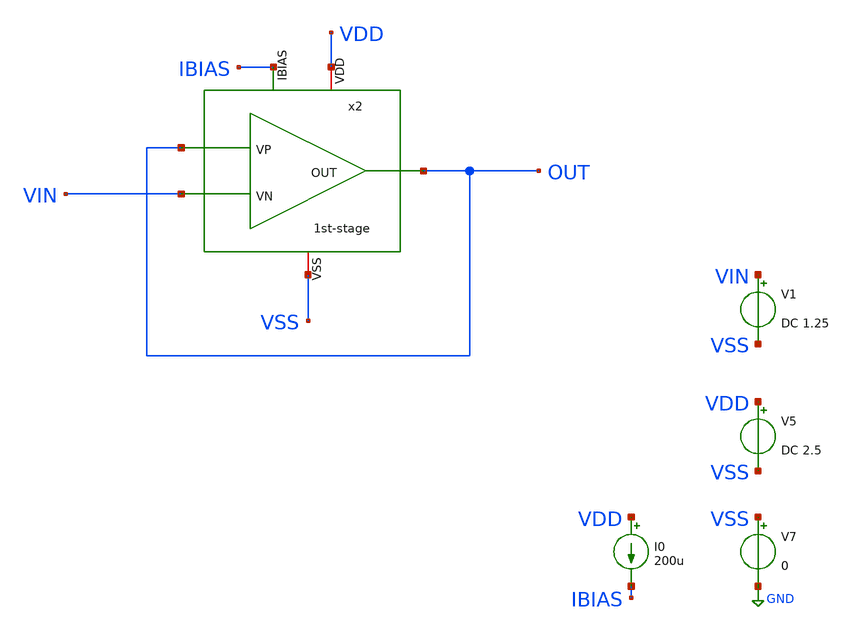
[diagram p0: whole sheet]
** sch_path: xschem/error-amplifier2/schematics/offset-mc.sch
**.subckt offset-mc
V5 VDD VSS DC 2.5
V7 VSS GND 0
x2 VDD OUT VIN OUT IBIAS VSS 1st-stage
I0 VDD IBIAS 200u
V1 VIN VSS DC 1.25
**** begin user architecture code



.control
  set noaskquit
  set wr_vecnames
  set wr_singlescale

  let mc_runs = 100
  let run = 0
  let vcm_target = 1.25

  * --- INIT VECTOR (100 entries) ---
  compose vos_vec values 0 0 0 0 0 0 0 0 0 0 0 0 0 0 0 0 0 0 0 0 0 0 0 0 0 0 0 0 0 0 0 0 0 0 0 0 0 0
+ 0 0 0 0 0 0 0 0 0 0 0 0 0 0 0 0 0 0 0 0 0 0 0 0 0 0 0 0 0 0 0 0 0 0 0 0 0 0 0 0 0 0 0 0 0 0 0 0 0 0 0
+ 0 0 0 0 0 0 0 0 0 0 0

  dowhile run < mc_runs
    reset

    * FIX ERROR SETSEED: Hitung dulu di variabel luar
    let current_seed = run + 1
    setseed $&current_seed

    * Jalankan DC Sweep (V1 adalah source yang di-sweep)
    dc V1 1.247 1.252 0.001

    * Ekstraksi nilai Vin saat crossing
    meas dc vin_at_vcm find v(vin) when v(out)=vcm_target

    * Hitung Vos dalam uV dan masukkan ke vector
    let vos_val = (vcm_target - vin_at_vcm) * 1e6
    let vos_vec[run] = vos_val

    echo Iteration: $&run | Vos: $&vos_val uV
    let run = run + 1
  end

  * =============================================================
  * RE-FIXED CSV OUTPUT BLOCK (INDEX EVALUATION)
  * =============================================================
  shell rm -f vos_results.csv
  shell echo run,vos_uv > vos_results.csv

  let i = 0
  dowhile i < mc_runs
    let tmp_vos = vos_vec[i]
    echo $&i, $&tmp_vos >> vos_results.csv
    let i = i + 1
  end

  echo ==========================================================
  echo SELESAI! Cek 'vos_results.csv' di folder lo sekarang.
  print mean(vos_vec) std(vos_vec)
  echo ==========================================================
.endc




** opencircuitdesign pdks install
.option wnflag=1
.param MC_SWITCH=1.0
.lib $::SKYWATER_MODELS/sky130.lib.spice mc


**** end user architecture code
**.ends

* expanding   symbol:  icdec-biomedical-pmic/xschem/error-amplifier2/schematics/1st-stage.sym # of
*+ pins=6
** sym_path: xschem/error-amplifier2/schematics/1st-stage.sym
** sch_path: xschem/error-amplifier2/schematics/1st-stage.sch
.subckt 1st-stage VDD OUT VN VP IBIAS VSS
*.iopin VDD
*.ipin VP
*.ipin VN
*.ipin IBIAS
*.iopin VSS
*.opin OUT
XM1 net2 net1 VDD VDD sky130_fd_pr__pfet_g5v0d10v5 L=1.25 W=75.2 nf=8 ad='int((nf+1)/2) * W/nf * 0.29'
+ as='int((nf+2)/2) * W/nf * 0.29' pd='2*int((nf+1)/2) * (W/nf + 0.29)' ps='2*int((nf+2)/2) * (W/nf + 0.29)'
+ nrd='0.29 / W' nrs='0.29 / W' sa=0 sb=0 sd=0 mult=1 m=1
XM2 net1 net1 VDD VDD sky130_fd_pr__pfet_g5v0d10v5 L=1.25 W=75.2 nf=8 ad='int((nf+1)/2) * W/nf * 0.29'
+ as='int((nf+2)/2) * W/nf * 0.29' pd='2*int((nf+1)/2) * (W/nf + 0.29)' ps='2*int((nf+2)/2) * (W/nf + 0.29)'
+ nrd='0.29 / W' nrs='0.29 / W' sa=0 sb=0 sd=0 mult=1 m=1
XM3 VDD VDD VDD VDD sky130_fd_pr__pfet_g5v0d10v5 L=0.5 W=18.8 nf=2 ad='int((nf+1)/2) * W/nf * 0.29' as='int((nf+2)/2) * W/nf * 0.29'
+ pd='2*int((nf+1)/2) * (W/nf + 0.29)' ps='2*int((nf+2)/2) * (W/nf + 0.29)' nrd='0.29 / W' nrs='0.29 / W'
+ sa=0 sb=0 sd=0 mult=1 m=1
XM4 VDD VDD VDD VDD sky130_fd_pr__pfet_g5v0d10v5 L=0.5 W=18.8 nf=2 ad='int((nf+1)/2) * W/nf * 0.29' as='int((nf+2)/2) * W/nf * 0.29'
+ pd='2*int((nf+1)/2) * (W/nf + 0.29)' ps='2*int((nf+2)/2) * (W/nf + 0.29)' nrd='0.29 / W' nrs='0.29 / W'
+ sa=0 sb=0 sd=0 mult=1 m=1
XM5 net2 VN net3 VSS sky130_fd_pr__nfet_g5v0d10v5 L=0.5 W=38 nf=2 ad='int((nf+1)/2) * W/nf * 0.29' as='int((nf+2)/2) * W/nf * 0.29'
+ pd='2*int((nf+1)/2) * (W/nf + 0.29)' ps='2*int((nf+2)/2) * (W/nf + 0.29)' nrd='0.29 / W' nrs='0.29 / W'
+ sa=0 sb=0 sd=0 mult=1 m=1
XM6 net1 VP net3 VSS sky130_fd_pr__nfet_g5v0d10v5 L=0.5 W=38 nf=2 ad='int((nf+1)/2) * W/nf * 0.29' as='int((nf+2)/2) * W/nf * 0.29'
+ pd='2*int((nf+1)/2) * (W/nf + 0.29)' ps='2*int((nf+2)/2) * (W/nf + 0.29)' nrd='0.29 / W' nrs='0.29 / W'
+ sa=0 sb=0 sd=0 mult=1 m=1
XM7 VSS VSS VSS VSS sky130_fd_pr__nfet_g5v0d10v5 L=0.5 W=9.5 nf=2 ad='int((nf+1)/2) * W/nf * 0.29' as='int((nf+2)/2) * W/nf * 0.29'
+ pd='2*int((nf+1)/2) * (W/nf + 0.29)' ps='2*int((nf+2)/2) * (W/nf + 0.29)' nrd='0.29 / W' nrs='0.29 / W'
+ sa=0 sb=0 sd=0 mult=1 m=1
XM8 VSS VSS VSS VSS sky130_fd_pr__nfet_g5v0d10v5 L=0.5 W=9.5 nf=2 ad='int((nf+1)/2) * W/nf * 0.29' as='int((nf+2)/2) * W/nf * 0.29'
+ pd='2*int((nf+1)/2) * (W/nf + 0.29)' ps='2*int((nf+2)/2) * (W/nf + 0.29)' nrd='0.29 / W' nrs='0.29 / W'
+ sa=0 sb=0 sd=0 mult=1 m=1
XM9 VSS VSS VSS VSS sky130_fd_pr__nfet_g5v0d10v5 L=0.5 W=9.5 nf=2 ad='int((nf+1)/2) * W/nf * 0.29' as='int((nf+2)/2) * W/nf * 0.29'
+ pd='2*int((nf+1)/2) * (W/nf + 0.29)' ps='2*int((nf+2)/2) * (W/nf + 0.29)' nrd='0.29 / W' nrs='0.29 / W'
+ sa=0 sb=0 sd=0 mult=1 m=1
XM10 VSS VSS VSS VSS sky130_fd_pr__nfet_g5v0d10v5 L=0.5 W=9.5 nf=2 ad='int((nf+1)/2) * W/nf * 0.29' as='int((nf+2)/2) * W/nf * 0.29'
+ pd='2*int((nf+1)/2) * (W/nf + 0.29)' ps='2*int((nf+2)/2) * (W/nf + 0.29)' nrd='0.29 / W' nrs='0.29 / W'
+ sa=0 sb=0 sd=0 mult=1 m=1
XM11 VSS VSS VSS VSS sky130_fd_pr__nfet_g5v0d10v5 L=0.5 W=9.5 nf=2 ad='int((nf+1)/2) * W/nf * 0.29' as='int((nf+2)/2) * W/nf * 0.29'
+ pd='2*int((nf+1)/2) * (W/nf + 0.29)' ps='2*int((nf+2)/2) * (W/nf + 0.29)' nrd='0.29 / W' nrs='0.29 / W'
+ sa=0 sb=0 sd=0 mult=1 m=1
XM12 VSS VSS VSS VSS sky130_fd_pr__nfet_g5v0d10v5 L=0.5 W=9.5 nf=2 ad='int((nf+1)/2) * W/nf * 0.29' as='int((nf+2)/2) * W/nf * 0.29'
+ pd='2*int((nf+1)/2) * (W/nf + 0.29)' ps='2*int((nf+2)/2) * (W/nf + 0.29)' nrd='0.29 / W' nrs='0.29 / W'
+ sa=0 sb=0 sd=0 mult=1 m=1
XM13 VSS VSS VSS VSS sky130_fd_pr__nfet_g5v0d10v5 L=0.5 W=9.5 nf=2 ad='int((nf+1)/2) * W/nf * 0.29' as='int((nf+2)/2) * W/nf * 0.29'
+ pd='2*int((nf+1)/2) * (W/nf + 0.29)' ps='2*int((nf+2)/2) * (W/nf + 0.29)' nrd='0.29 / W' nrs='0.29 / W'
+ sa=0 sb=0 sd=0 mult=1 m=1
XM14 VSS VSS VSS VSS sky130_fd_pr__nfet_g5v0d10v5 L=0.5 W=9.5 nf=2 ad='int((nf+1)/2) * W/nf * 0.29' as='int((nf+2)/2) * W/nf * 0.29'
+ pd='2*int((nf+1)/2) * (W/nf + 0.29)' ps='2*int((nf+2)/2) * (W/nf + 0.29)' nrd='0.29 / W' nrs='0.29 / W'
+ sa=0 sb=0 sd=0 mult=1 m=1
XM15 VSS VSS VSS VSS sky130_fd_pr__nfet_g5v0d10v5 L=0.5 W=9.5 nf=2 ad='int((nf+1)/2) * W/nf * 0.29' as='int((nf+2)/2) * W/nf * 0.29'
+ pd='2*int((nf+1)/2) * (W/nf + 0.29)' ps='2*int((nf+2)/2) * (W/nf + 0.29)' nrd='0.29 / W' nrs='0.29 / W'
+ sa=0 sb=0 sd=0 mult=1 m=1
XM16 VSS VSS VSS VSS sky130_fd_pr__nfet_g5v0d10v5 L=0.5 W=9.5 nf=2 ad='int((nf+1)/2) * W/nf * 0.29' as='int((nf+2)/2) * W/nf * 0.29'
+ pd='2*int((nf+1)/2) * (W/nf + 0.29)' ps='2*int((nf+2)/2) * (W/nf + 0.29)' nrd='0.29 / W' nrs='0.29 / W'
+ sa=0 sb=0 sd=0 mult=1 m=1
XM17 VSS VSS VSS VSS sky130_fd_pr__nfet_g5v0d10v5 L=0.5 W=9.5 nf=2 ad='int((nf+1)/2) * W/nf * 0.29' as='int((nf+2)/2) * W/nf * 0.29'
+ pd='2*int((nf+1)/2) * (W/nf + 0.29)' ps='2*int((nf+2)/2) * (W/nf + 0.29)' nrd='0.29 / W' nrs='0.29 / W'
+ sa=0 sb=0 sd=0 mult=1 m=1
XM18 VSS VSS VSS VSS sky130_fd_pr__nfet_g5v0d10v5 L=0.5 W=9.5 nf=2 ad='int((nf+1)/2) * W/nf * 0.29' as='int((nf+2)/2) * W/nf * 0.29'
+ pd='2*int((nf+1)/2) * (W/nf + 0.29)' ps='2*int((nf+2)/2) * (W/nf + 0.29)' nrd='0.29 / W' nrs='0.29 / W'
+ sa=0 sb=0 sd=0 mult=1 m=1
XM19 VSS VSS VSS VSS sky130_fd_pr__nfet_g5v0d10v5 L=0.5 W=9.5 nf=2 ad='int((nf+1)/2) * W/nf * 0.29' as='int((nf+2)/2) * W/nf * 0.29'
+ pd='2*int((nf+1)/2) * (W/nf + 0.29)' ps='2*int((nf+2)/2) * (W/nf + 0.29)' nrd='0.29 / W' nrs='0.29 / W'
+ sa=0 sb=0 sd=0 mult=1 m=1
XM20 VSS VSS VSS VSS sky130_fd_pr__nfet_g5v0d10v5 L=0.5 W=9.5 nf=2 ad='int((nf+1)/2) * W/nf * 0.29' as='int((nf+2)/2) * W/nf * 0.29'
+ pd='2*int((nf+1)/2) * (W/nf + 0.29)' ps='2*int((nf+2)/2) * (W/nf + 0.29)' nrd='0.29 / W' nrs='0.29 / W'
+ sa=0 sb=0 sd=0 mult=1 m=1
XM21 VSS VSS VSS VSS sky130_fd_pr__nfet_g5v0d10v5 L=0.5 W=9.5 nf=2 ad='int((nf+1)/2) * W/nf * 0.29' as='int((nf+2)/2) * W/nf * 0.29'
+ pd='2*int((nf+1)/2) * (W/nf + 0.29)' ps='2*int((nf+2)/2) * (W/nf + 0.29)' nrd='0.29 / W' nrs='0.29 / W'
+ sa=0 sb=0 sd=0 mult=1 m=1
XM22 VSS VSS VSS VSS sky130_fd_pr__nfet_g5v0d10v5 L=0.5 W=9.5 nf=2 ad='int((nf+1)/2) * W/nf * 0.29' as='int((nf+2)/2) * W/nf * 0.29'
+ pd='2*int((nf+1)/2) * (W/nf + 0.29)' ps='2*int((nf+2)/2) * (W/nf + 0.29)' nrd='0.29 / W' nrs='0.29 / W'
+ sa=0 sb=0 sd=0 mult=1 m=1
XM23 net3 IBIAS VSS VSS sky130_fd_pr__nfet_g5v0d10v5 L=1.25 W=60 nf=4 ad='int((nf+1)/2) * W/nf * 0.29'
+ as='int((nf+2)/2) * W/nf * 0.29' pd='2*int((nf+1)/2) * (W/nf + 0.29)' ps='2*int((nf+2)/2) * (W/nf + 0.29)'
+ nrd='0.29 / W' nrs='0.29 / W' sa=0 sb=0 sd=0 mult=1 m=1
XM24 IBIAS IBIAS VSS VSS sky130_fd_pr__nfet_g5v0d10v5 L=1.25 W=60 nf=4 ad='int((nf+1)/2) * W/nf * 0.29'
+ as='int((nf+2)/2) * W/nf * 0.29' pd='2*int((nf+1)/2) * (W/nf + 0.29)' ps='2*int((nf+2)/2) * (W/nf + 0.29)'
+ nrd='0.29 / W' nrs='0.29 / W' sa=0 sb=0 sd=0 mult=1 m=1
XM25 VSS VSS VSS VSS sky130_fd_pr__nfet_g5v0d10v5 L=0.5 W=15 nf=2 ad='int((nf+1)/2) * W/nf * 0.29' as='int((nf+2)/2) * W/nf * 0.29'
+ pd='2*int((nf+1)/2) * (W/nf + 0.29)' ps='2*int((nf+2)/2) * (W/nf + 0.29)' nrd='0.29 / W' nrs='0.29 / W'
+ sa=0 sb=0 sd=0 mult=1 m=1
XM26 VSS VSS VSS VSS sky130_fd_pr__nfet_g5v0d10v5 L=0.5 W=15 nf=2 ad='int((nf+1)/2) * W/nf * 0.29' as='int((nf+2)/2) * W/nf * 0.29'
+ pd='2*int((nf+1)/2) * (W/nf + 0.29)' ps='2*int((nf+2)/2) * (W/nf + 0.29)' nrd='0.29 / W' nrs='0.29 / W'
+ sa=0 sb=0 sd=0 mult=1 m=1
XM27 OUT net2 VDD VDD sky130_fd_pr__pfet_g5v0d10v5 L=1.25 W=160 nf=16 ad='int((nf+1)/2) * W/nf * 0.29'
+ as='int((nf+2)/2) * W/nf * 0.29' pd='2*int((nf+1)/2) * (W/nf + 0.29)' ps='2*int((nf+2)/2) * (W/nf + 0.29)'
+ nrd='0.29 / W' nrs='0.29 / W' sa=0 sb=0 sd=0 mult=1 m=1
XM28 OUT IBIAS VSS VSS sky130_fd_pr__nfet_g5v0d10v5 L=1.25 W=60 nf=8 ad='int((nf+1)/2) * W/nf * 0.29'
+ as='int((nf+2)/2) * W/nf * 0.29' pd='2*int((nf+1)/2) * (W/nf + 0.29)' ps='2*int((nf+2)/2) * (W/nf + 0.29)'
+ nrd='0.29 / W' nrs='0.29 / W' sa=0 sb=0 sd=0 mult=1 m=1
XC1 net4 net2 sky130_fd_pr__cap_mim_m3_1 W=25 L=25 MF=8 m=8
XM29 OUT VSS net4 VDD sky130_fd_pr__pfet_g5v0d10v5 L=0.9 W=20 nf=4 ad='int((nf+1)/2) * W/nf * 0.29' as='int((nf+2)/2) * W/nf * 0.29'
+ pd='2*int((nf+1)/2) * (W/nf + 0.29)' ps='2*int((nf+2)/2) * (W/nf + 0.29)' nrd='0.29 / W' nrs='0.29 / W'
+ sa=0 sb=0 sd=0 mult=1 m=1
.ends

.GLOBAL GND
.end
